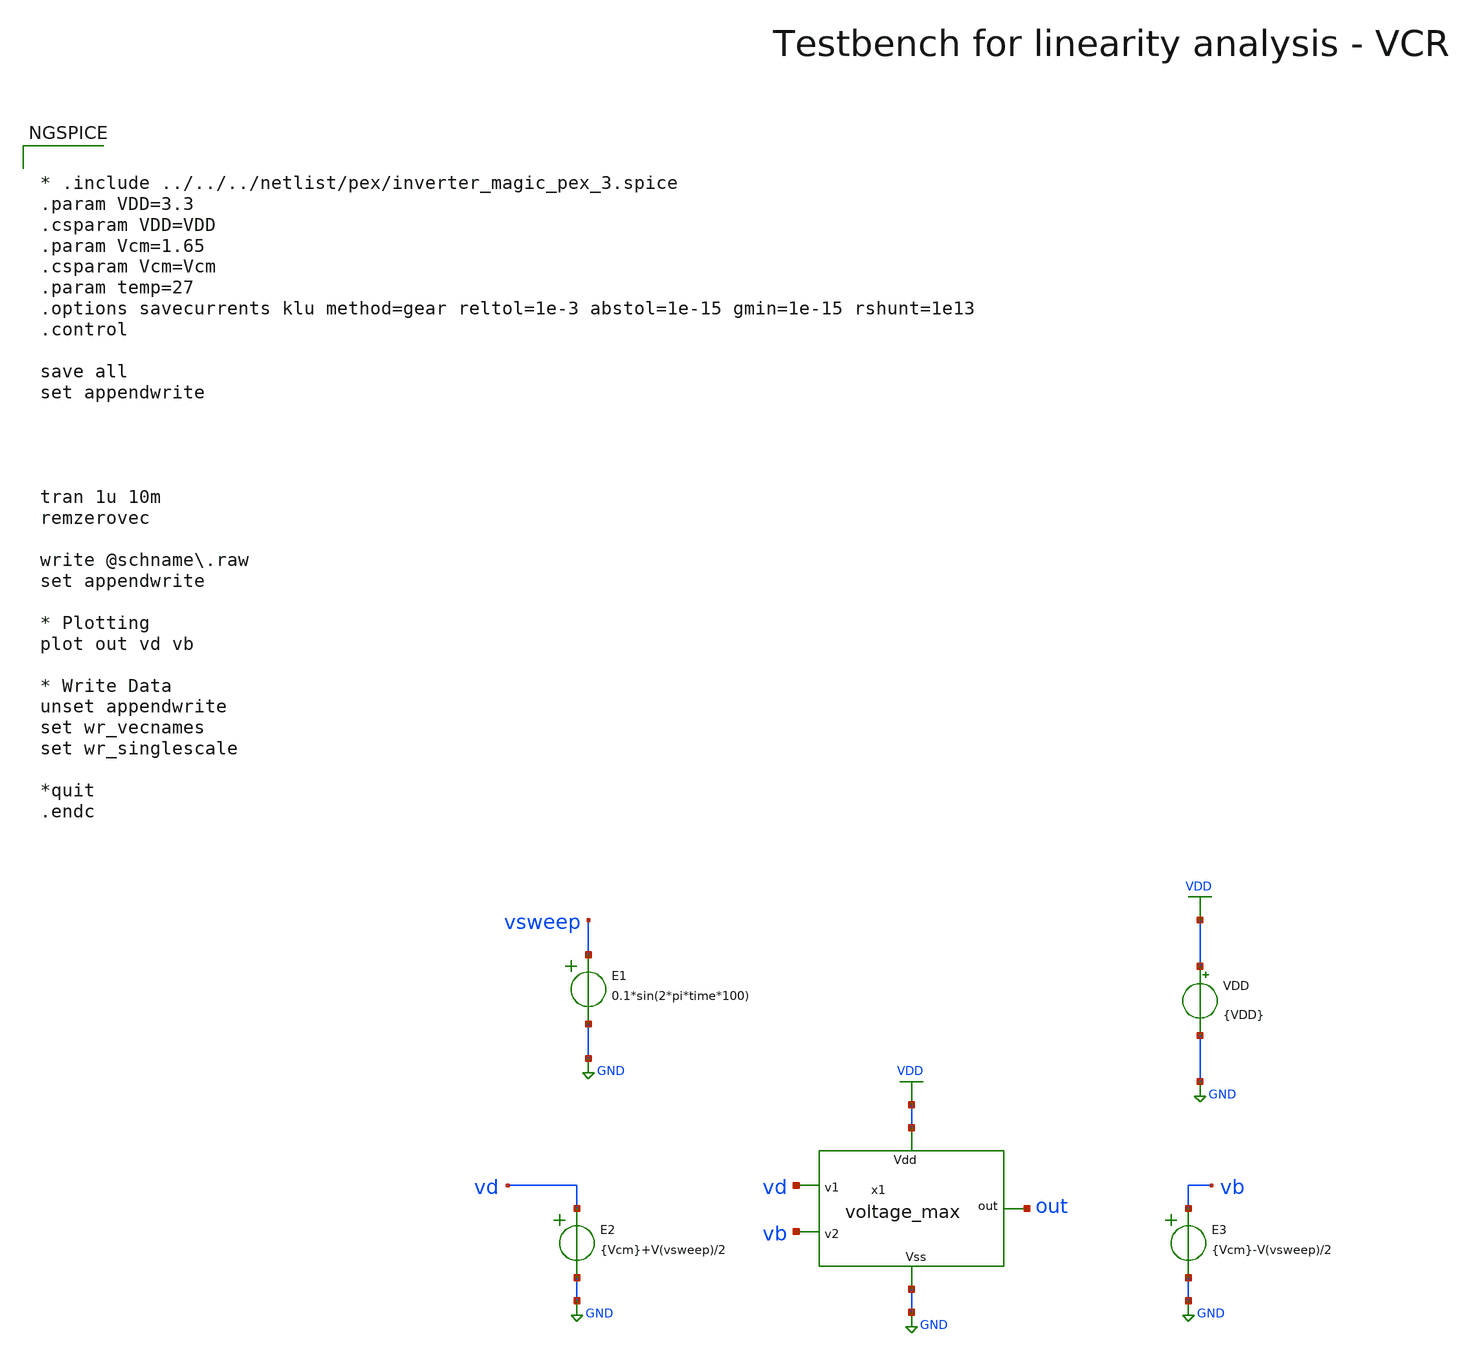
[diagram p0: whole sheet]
** sch_path: macros/heichips26_vcr/macros/vcr_bisection/testbenches/xschem/vmax_tb_tran.sch
**.subckt vmax_tb_tran
VDD VDD GND {VDD}
E2 vd GND VOL=' {Vcm}+V(vsweep)/2 '
E3 vb GND VOL=' {Vcm}-V(vsweep)/2 '
x1 vd VDD GND out vb voltage_max
E1 vsweep GND VOL=' 0.1*sin(2*pi*time*100) '
**** begin user architecture code

.lib cornerMOSlv.lib mos_tt
.lib cornerMOShv.lib mos_tt
.lib cornerRES.lib res_typ
.lib cornerDIO.lib dio_tt
.lib cornerCAP.lib cap_typ



* .include ../../../netlist/pex/inverter_magic_pex_3.spice
.param VDD=3.3
.csparam VDD=VDD
.param Vcm=1.65
.csparam Vcm=Vcm
.param temp=27
.options savecurrents klu method=gear reltol=1e-3 abstol=1e-15 gmin=1e-15 rshunt=1e13
.control

save all
set appendwrite




tran 1u 10m
remzerovec

write @schname\.raw
set appendwrite

* Plotting
plot out vd vb

* Write Data
unset appendwrite
set wr_vecnames
set wr_singlescale

*quit
.endc


**** end user architecture code
**.ends
.GLOBAL GND
.GLOBAL VDD
.end
